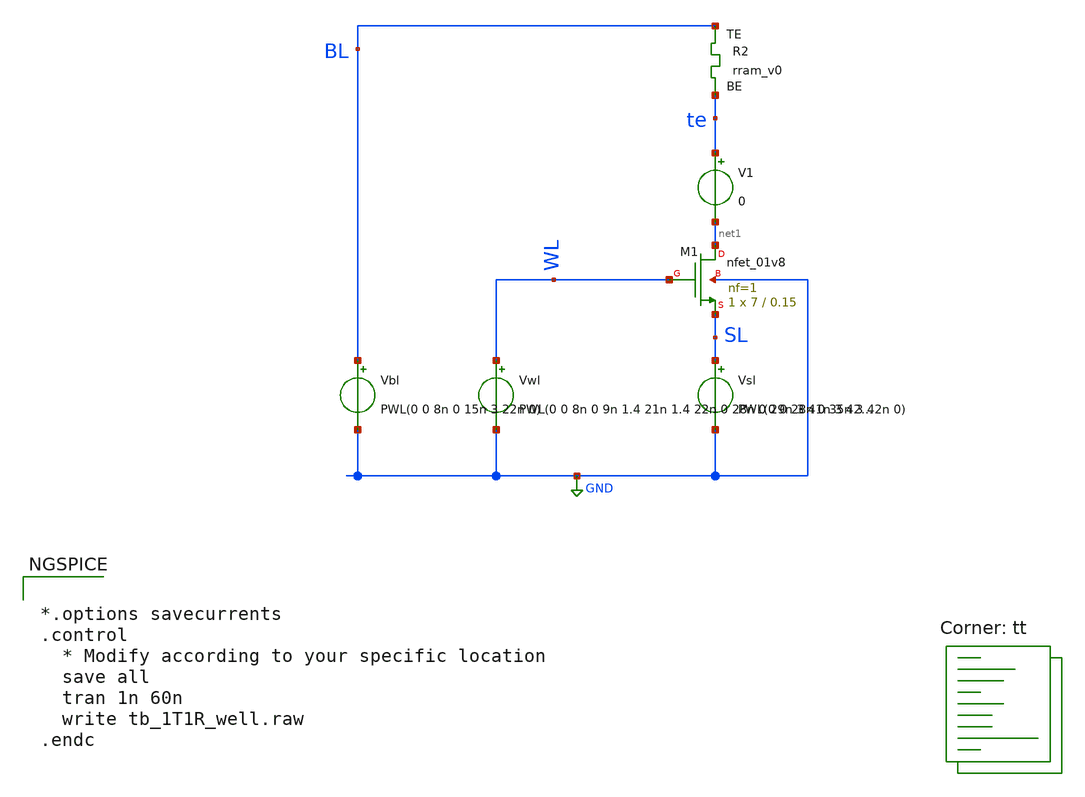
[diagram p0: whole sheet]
** sch_path: memristor_models/wellposed/tb_1T1R_well.sch
**.subckt tb_1T1R_well
XM1 net1 WL SL GND sky130_fd_pr__nfet_01v8 L=0.15 W=7 nf=1 ad='int((nf+1)/2) * W/nf * 0.29' as='int((nf+2)/2) * W/nf * 0.29'
+ pd='2*int((nf+1)/2) * (W/nf + 0.29)' ps='2*int((nf+2)/2) * (W/nf + 0.29)' nrd='0.29 / W' nrs='0.29 / W'
+ sa=0 sb=0 sd=0 mult=1 m=1
Vwl WL GND PWL(0 0 8n 0 9n 1.4 21n 1.4 22n 0 28n 0 29n 3 41n 3 42n 0)
Vbl BL GND PWL(0 0 8n 0 15n 3 22n 0)
V1 te net1 0
Vsl SL GND PWL(0 0 28n 0 35n 3 42n 0)
XR2 BL te rram_v0
**** begin user architecture code


*.options savecurrents
.control
  * Modify according to your specific location
  save all
  tran 1n 60n
  write tb_1T1R_well.raw
.endc



.lib $::SKYWATER_MODELS/sky130.lib.spice tt

** opencircuitdesign pdks install
.inc $::SKYWATER_MODELS/rram_v0.spice

**** end user architecture code
**.ends
.GLOBAL GND
.end
